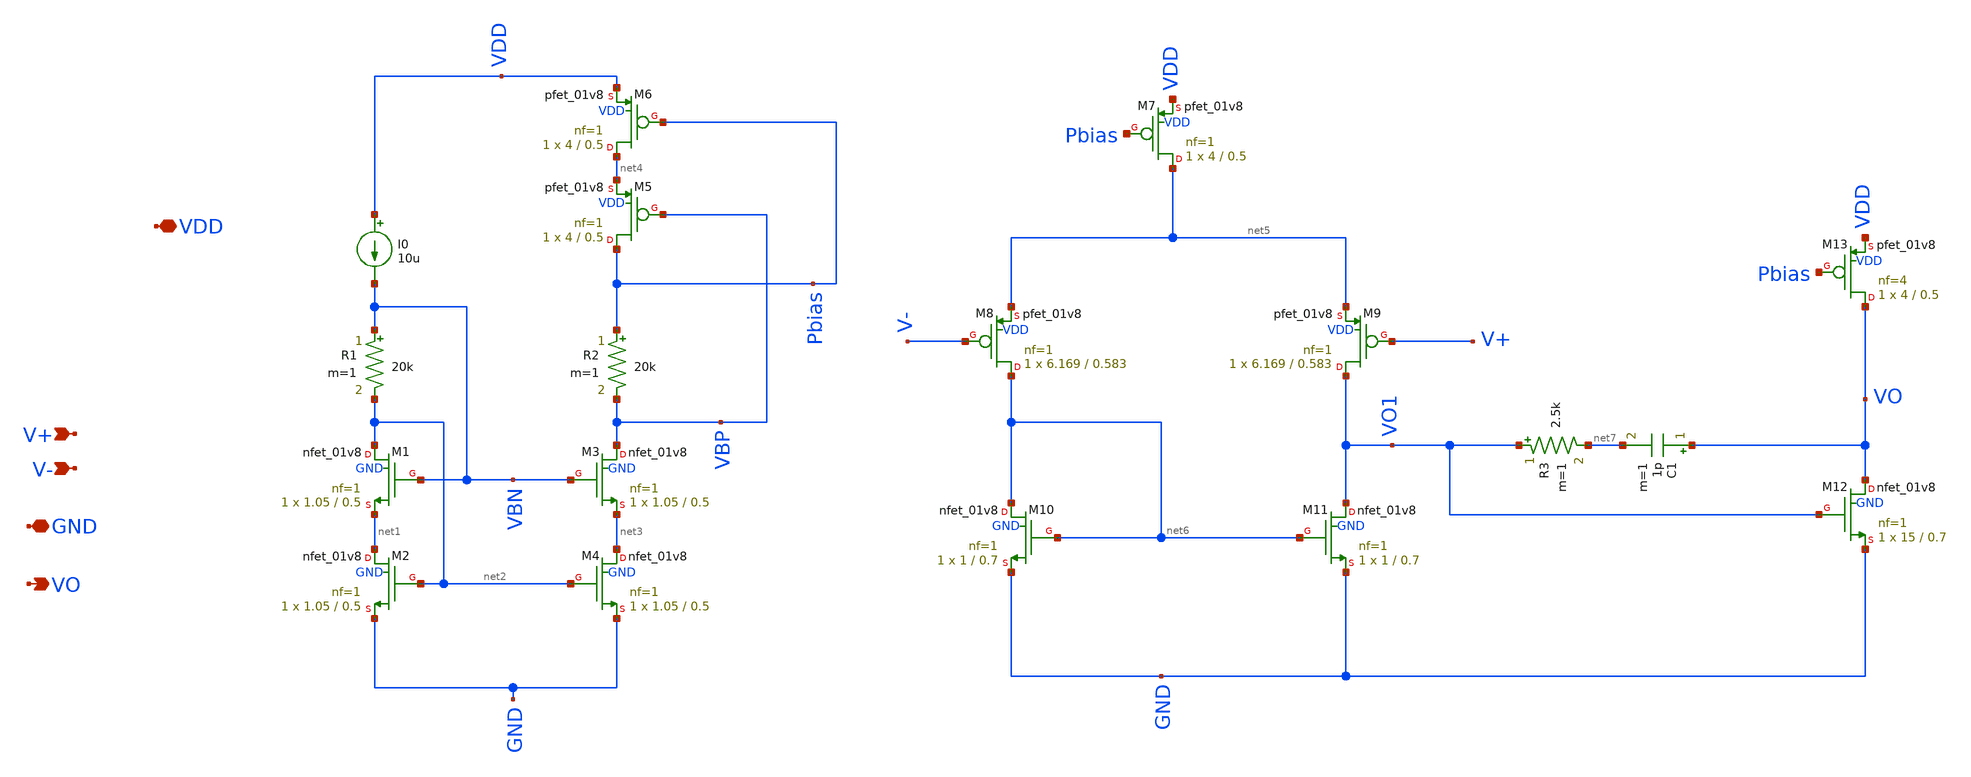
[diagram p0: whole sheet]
** sch_path: pll/pfd_cp_lf_lib/OTA/xschem/5TOTA.sch
**.subckt 5TOTA V+ V- VO GND VDD
*.ipin V+
*.ipin V-
*.opin VO
*.iopin GND
*.iopin VDD
XM1 net2 VBN net1 GND sky130_fd_pr__nfet_01v8 L=0.5 W=1.05 nf=1 ad='int((nf+1)/2) * W/nf * 0.29' as='int((nf+2)/2) * W/nf * 0.29'
+ pd='2*int((nf+1)/2) * (W/nf + 0.29)' ps='2*int((nf+2)/2) * (W/nf + 0.29)' nrd='0.29 / W' nrs='0.29 / W'
+ sa=0 sb=0 sd=0 mult=1 m=1
XM2 net1 net2 GND GND sky130_fd_pr__nfet_01v8 L=0.5 W=1.05 nf=1 ad='int((nf+1)/2) * W/nf * 0.29' as='int((nf+2)/2) * W/nf * 0.29'
+ pd='2*int((nf+1)/2) * (W/nf + 0.29)' ps='2*int((nf+2)/2) * (W/nf + 0.29)' nrd='0.29 / W' nrs='0.29 / W'
+ sa=0 sb=0 sd=0 mult=1 m=1
XM3 VBP VBN net3 GND sky130_fd_pr__nfet_01v8 L=0.5 W=1.05 nf=1 ad='int((nf+1)/2) * W/nf * 0.29' as='int((nf+2)/2) * W/nf * 0.29'
+ pd='2*int((nf+1)/2) * (W/nf + 0.29)' ps='2*int((nf+2)/2) * (W/nf + 0.29)' nrd='0.29 / W' nrs='0.29 / W'
+ sa=0 sb=0 sd=0 mult=1 m=1
XM4 net3 net2 GND GND sky130_fd_pr__nfet_01v8 L=0.5 W=1.05 nf=1 ad='int((nf+1)/2) * W/nf * 0.29' as='int((nf+2)/2) * W/nf * 0.29'
+ pd='2*int((nf+1)/2) * (W/nf + 0.29)' ps='2*int((nf+2)/2) * (W/nf + 0.29)' nrd='0.29 / W' nrs='0.29 / W'
+ sa=0 sb=0 sd=0 mult=1 m=1
R1 VBN net2 20k m=1
R2 Pbias VBP 20k m=1
I0 VDD VBN 10u
XM5 Pbias VBP net4 VDD sky130_fd_pr__pfet_01v8 L=0.5 W=4 nf=1 ad='int((nf+1)/2) * W/nf * 0.29' as='int((nf+2)/2) * W/nf * 0.29'
+ pd='2*int((nf+1)/2) * (W/nf + 0.29)' ps='2*int((nf+2)/2) * (W/nf + 0.29)' nrd='0.29 / W' nrs='0.29 / W'
+ sa=0 sb=0 sd=0 mult=1 m=1
XM6 net4 Pbias VDD VDD sky130_fd_pr__pfet_01v8 L=0.5 W=4 nf=1 ad='int((nf+1)/2) * W/nf * 0.29' as='int((nf+2)/2) * W/nf * 0.29'
+ pd='2*int((nf+1)/2) * (W/nf + 0.29)' ps='2*int((nf+2)/2) * (W/nf + 0.29)' nrd='0.29 / W' nrs='0.29 / W'
+ sa=0 sb=0 sd=0 mult=1 m=1
XM7 net5 Pbias VDD VDD sky130_fd_pr__pfet_01v8 L=0.5 W=4 nf=1 ad='int((nf+1)/2) * W/nf * 0.29' as='int((nf+2)/2) * W/nf * 0.29'
+ pd='2*int((nf+1)/2) * (W/nf + 0.29)' ps='2*int((nf+2)/2) * (W/nf + 0.29)' nrd='0.29 / W' nrs='0.29 / W'
+ sa=0 sb=0 sd=0 mult=1 m=1
XM8 net6 V- net5 VDD sky130_fd_pr__pfet_01v8 L=0.583 W=6.169 nf=1 ad='int((nf+1)/2) * W/nf * 0.29' as='int((nf+2)/2) * W/nf * 0.29'
+ pd='2*int((nf+1)/2) * (W/nf + 0.29)' ps='2*int((nf+2)/2) * (W/nf + 0.29)' nrd='0.29 / W' nrs='0.29 / W'
+ sa=0 sb=0 sd=0 mult=1 m=1
XM9 VO1 V+ net5 VDD sky130_fd_pr__pfet_01v8 L=0.583 W=6.169 nf=1 ad='int((nf+1)/2) * W/nf * 0.29' as='int((nf+2)/2) * W/nf * 0.29'
+ pd='2*int((nf+1)/2) * (W/nf + 0.29)' ps='2*int((nf+2)/2) * (W/nf + 0.29)' nrd='0.29 / W' nrs='0.29 / W'
+ sa=0 sb=0 sd=0 mult=1 m=1
XM10 net6 net6 GND GND sky130_fd_pr__nfet_01v8 L=0.7 W=1 nf=1 ad='int((nf+1)/2) * W/nf * 0.29' as='int((nf+2)/2) * W/nf * 0.29'
+ pd='2*int((nf+1)/2) * (W/nf + 0.29)' ps='2*int((nf+2)/2) * (W/nf + 0.29)' nrd='0.29 / W' nrs='0.29 / W'
+ sa=0 sb=0 sd=0 mult=1 m=1
XM11 VO1 net6 GND GND sky130_fd_pr__nfet_01v8 L=0.7 W=1 nf=1 ad='int((nf+1)/2) * W/nf * 0.29' as='int((nf+2)/2) * W/nf * 0.29'
+ pd='2*int((nf+1)/2) * (W/nf + 0.29)' ps='2*int((nf+2)/2) * (W/nf + 0.29)' nrd='0.29 / W' nrs='0.29 / W'
+ sa=0 sb=0 sd=0 mult=1 m=1
R3 VO1 net7 2.5k m=1
C1 VO net7 1p m=1
XM12 VO VO1 GND GND sky130_fd_pr__nfet_01v8 L=0.7 W=15 nf=1 ad='int((nf+1)/2) * W/nf * 0.29' as='int((nf+2)/2) * W/nf * 0.29'
+ pd='2*int((nf+1)/2) * (W/nf + 0.29)' ps='2*int((nf+2)/2) * (W/nf + 0.29)' nrd='0.29 / W' nrs='0.29 / W'
+ sa=0 sb=0 sd=0 mult=1 m=1
XM13 VO Pbias VDD VDD sky130_fd_pr__pfet_01v8 L=0.5 W=4 nf=4 ad='int((nf+1)/2) * W/nf * 0.29' as='int((nf+2)/2) * W/nf * 0.29'
+ pd='2*int((nf+1)/2) * (W/nf + 0.29)' ps='2*int((nf+2)/2) * (W/nf + 0.29)' nrd='0.29 / W' nrs='0.29 / W'
+ sa=0 sb=0 sd=0 mult=1 m=1
**.ends
.end
